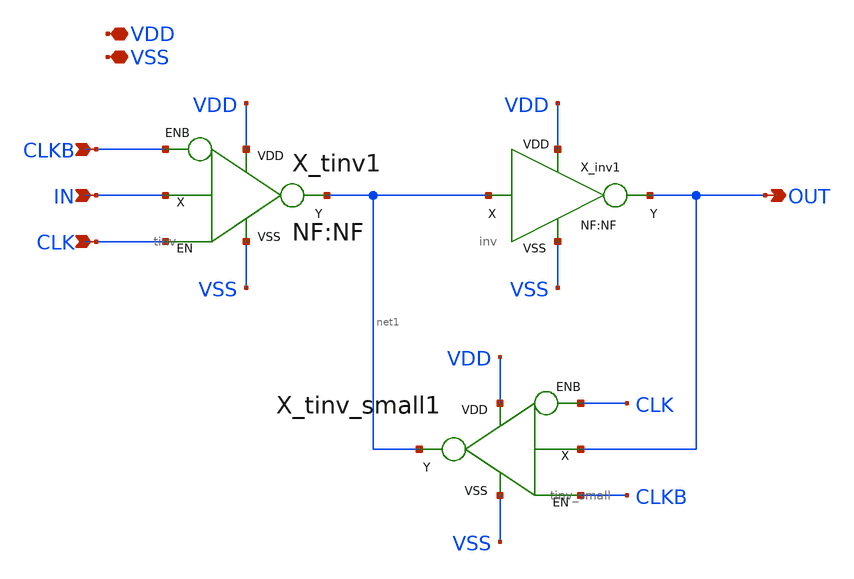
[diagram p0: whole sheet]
** sch_path: xschem_lib/DFFRAM_full_custom/latch.sch
**.subckt latch CLKB IN CLK VDD VSS OUT
*.ipin CLKB
*.ipin IN
*.ipin CLK
*.iopin VDD
*.iopin VSS
*.opin OUT
X_tinv1 IN CLK CLKB VDD VSS net1 tinv NF=NF
X_inv1 net1 VDD VSS OUT inv NF=NF
X_tinv_small1 OUT CLKB CLK VDD VSS net1 tinv_small
**.ends
.end
